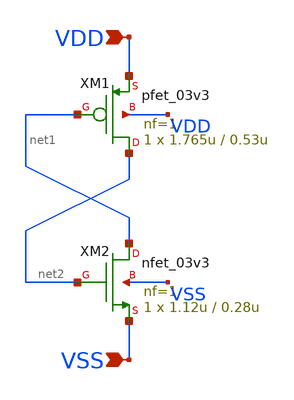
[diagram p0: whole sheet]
** sch_path: xschem/gf180mcu_ocd_sc_rt12t3v3__decap_4.sch
**.subckt gf180mcu_ocd_sc_rt12t3v3__decap_4 VDD VSS
*.ipin VDD
*.ipin VSS
XM1 net2 net1 VDD VDD pfet_03v3 L=0.53u W=1.765u nf=1 ad='int((nf+1)/2) * W/nf * 0.18u' as='int((nf+2)/2) * W/nf * 0.18u'
+ pd='2*int((nf+1)/2) * (W/nf + 0.18u)' ps='2*int((nf+2)/2) * (W/nf + 0.18u)' nrd='0.18u / W' nrs='0.18u / W'
+ sa=0 sb=0 sd=0 m=1
XM2 net1 net2 VSS VSS nfet_03v3 L=0.28u W=1.12u nf=1 ad='int((nf+1)/2) * W/nf * 0.18u' as='int((nf+2)/2) * W/nf * 0.18u'
+ pd='2*int((nf+1)/2) * (W/nf + 0.18u)' ps='2*int((nf+2)/2) * (W/nf + 0.18u)' nrd='0.18u / W' nrs='0.18u / W'
+ sa=0 sb=0 sd=0 m=1
**.ends
.end
